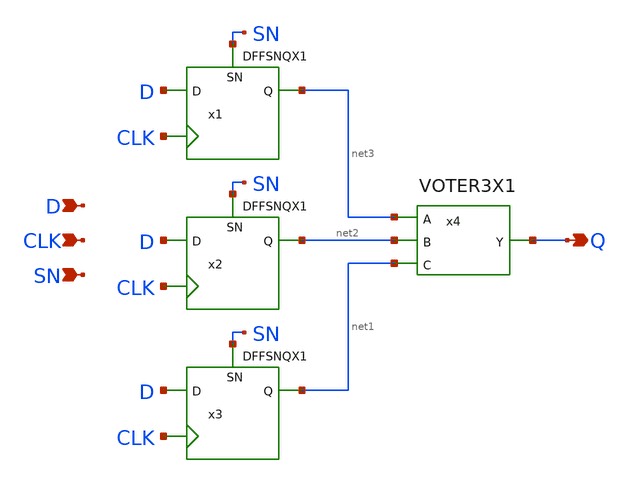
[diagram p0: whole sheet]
** sch_path: current/xschem/TMRDFFSNQX1.sch
**.subckt TMRDFFSNQX1 Q D CLK SN
*.opin Q
*.ipin D
*.ipin CLK
*.ipin SN
x4 Q net3 net2 net1 VDD VSS VOTER3X1
x1 net3 D CLK SN VDD VSS DFFSNQX1
x2 net2 D CLK SN VDD VSS DFFSNQX1
x3 net1 D CLK SN VDD VSS DFFSNQX1
**.ends
.end
